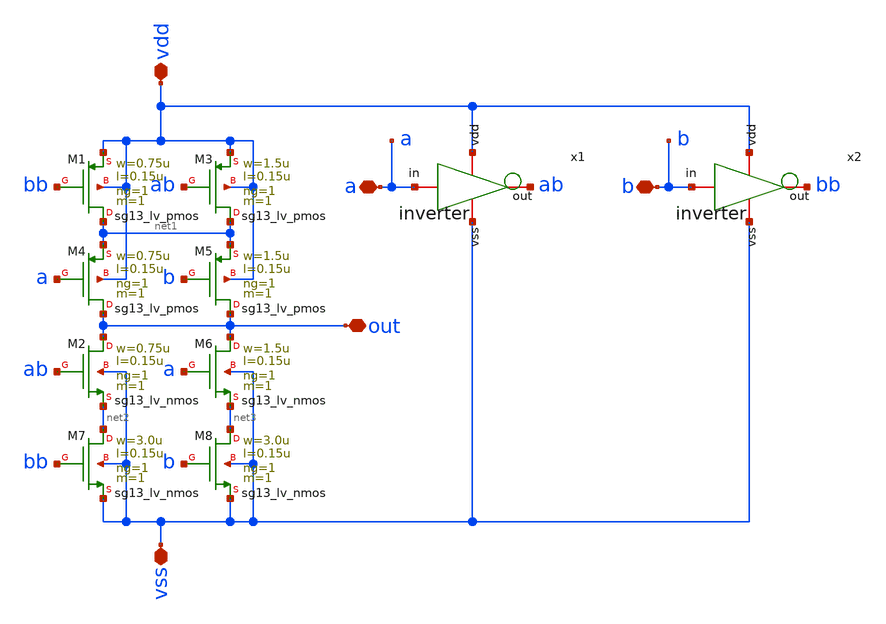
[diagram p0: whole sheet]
** sch_path: design/blocks/xorgate/schematic/xor.sch
**.subckt xor vss vdd a b out
*.iopin vss
*.iopin vdd
*.iopin a
*.iopin b
*.iopin out
XM1 net1 bb vdd vdd sg13_lv_pmos w=0.75u l=0.15u ng=1 m=1 mm_ok=1
XM2 out ab net2 vss sg13_lv_nmos w=0.75u l=0.15u ng=1 m=1 mm_ok=1
XM3 net1 ab vdd vdd sg13_lv_pmos w=1.5u l=0.15u ng=1 m=1 mm_ok=1
XM4 out a net1 vdd sg13_lv_pmos w=0.75u l=0.15u ng=1 m=1 mm_ok=1
XM5 out b net1 vdd sg13_lv_pmos w=1.5u l=0.15u ng=1 m=1 mm_ok=1
XM6 out a net3 vss sg13_lv_nmos w=1.5u l=0.15u ng=1 m=1 mm_ok=1
x1 vdd ab a vss inverter
x2 vdd bb b vss inverter
XM7 net2 bb vss vss sg13_lv_nmos w=3.0u l=0.15u ng=1 m=1 mm_ok=1
XM8 net3 b vss vss sg13_lv_nmos w=3.0u l=0.15u ng=1 m=1 mm_ok=1
**.ends

* expanding   symbol:  blocks/inverter/schematic/inverter.sym # of pins=4
** sym_path: design/blocks/inverter/schematic/inverter.sym
** sch_path: design/blocks/inverter/schematic/inverter.sch
.subckt inverter vdd out in vss
*.iopin vdd
*.iopin out
*.iopin vss
*.iopin in
XM1 out in vss vss sg13_lv_nmos w=0.75u l=0.15u ng=1 m=1 mm_ok=1
XM2 out in vdd vdd sg13_lv_pmos w=1.5u l=0.15u ng=1 m=1 mm_ok=1
.ends

.end
